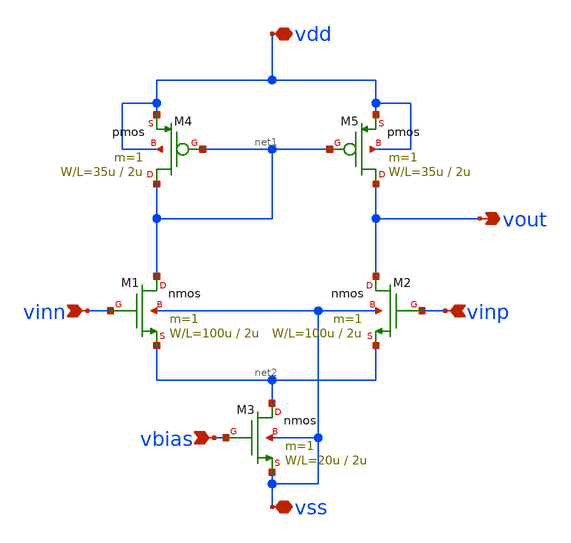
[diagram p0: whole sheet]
** sch_path: member_project/GroupWork/Team_masahiro/diff.sch
**.subckt diff vss vdd vinn vinp vout vbias
*.iopin vss
*.iopin vdd
*.ipin vinn
*.ipin vinp
*.opin vout
*.ipin vbias
M1 net1 vinn net2 vss nmos L=2u W=100u m=1
M2 vout vinp net2 vss nmos L=2u W=100u m=1
M3 net2 vbias vss vss nmos L=2u W=20u m=1
M4 net1 net1 vdd vdd pmos L=2u W=35u m=1
M5 vout net1 vdd vdd pmos L=2u W=35u m=1
**** begin user architecture code
 .include $::LIB/mos.lib
.include $::LIB/passive.lib
.include $::LIB/diode.lib
**** end user architecture code
**.ends
.end
